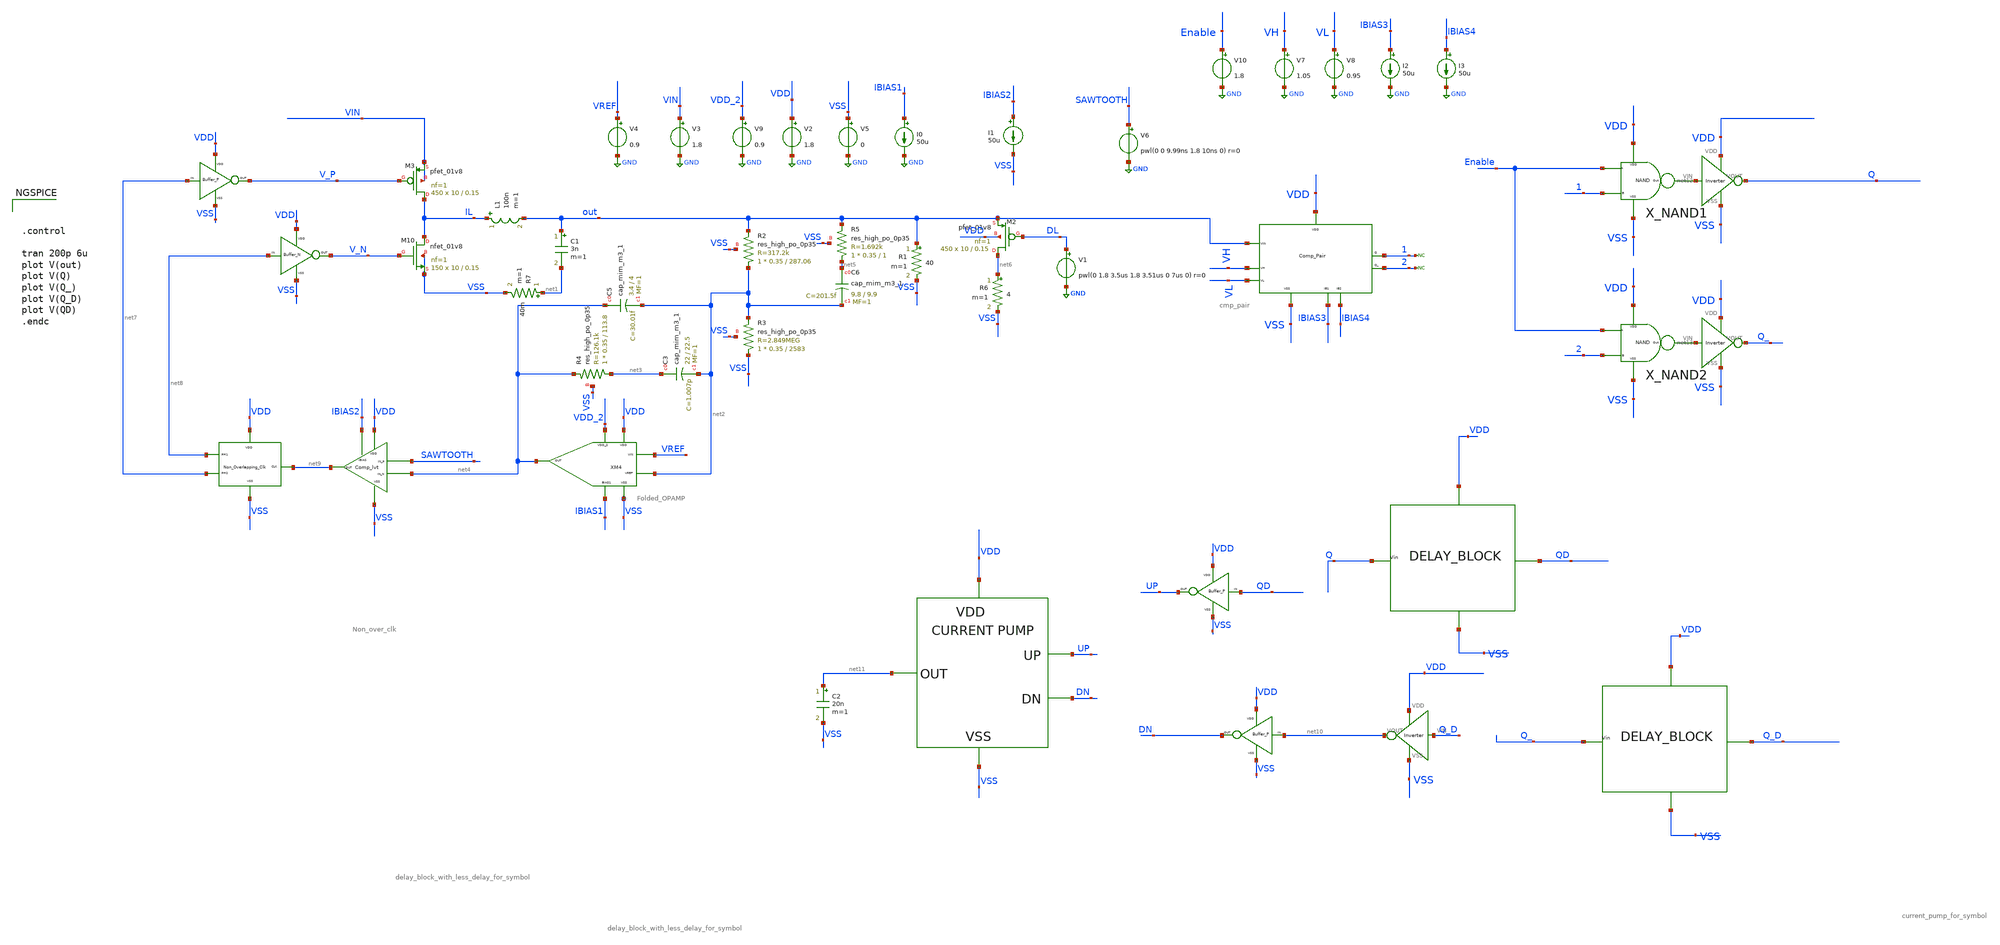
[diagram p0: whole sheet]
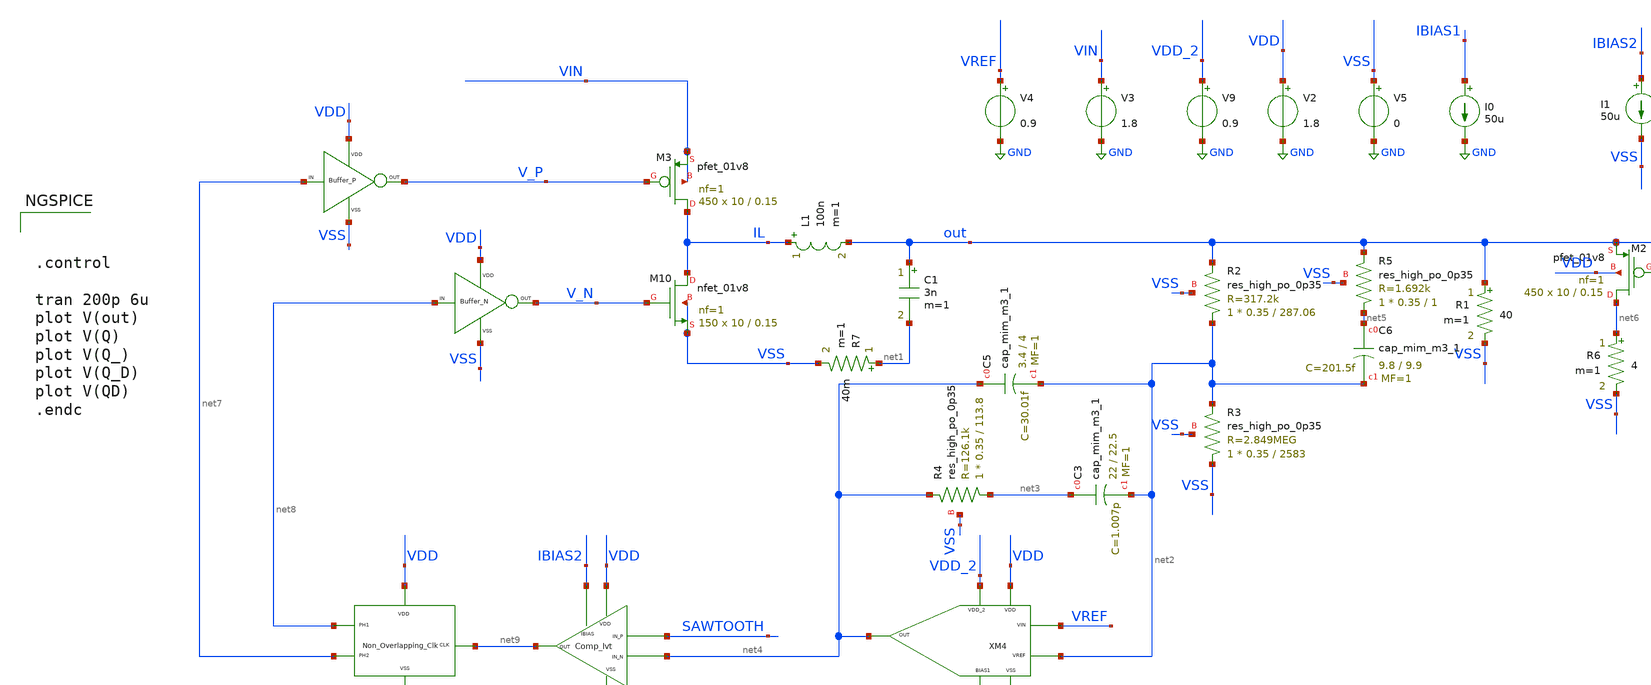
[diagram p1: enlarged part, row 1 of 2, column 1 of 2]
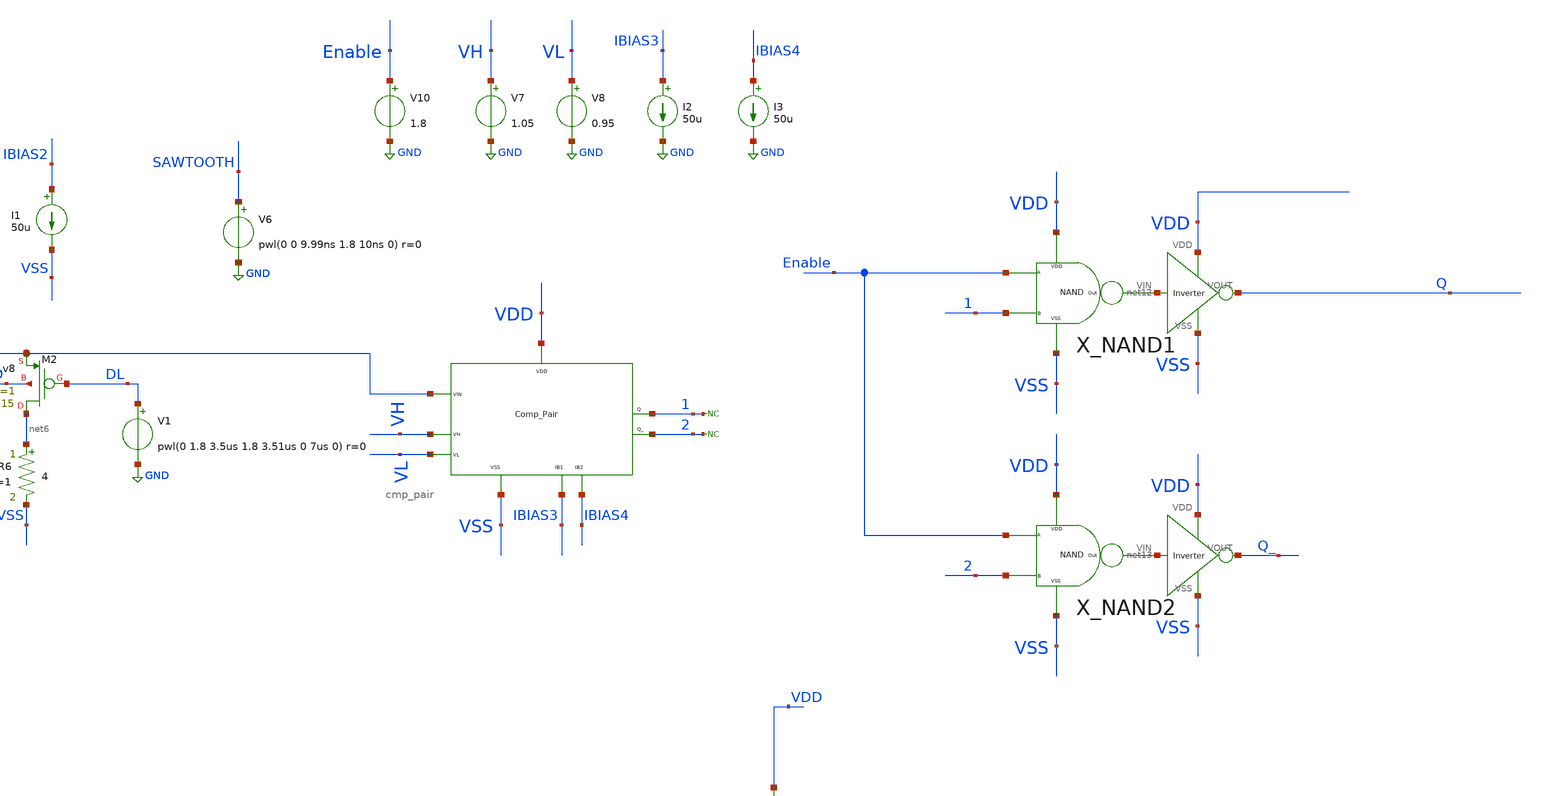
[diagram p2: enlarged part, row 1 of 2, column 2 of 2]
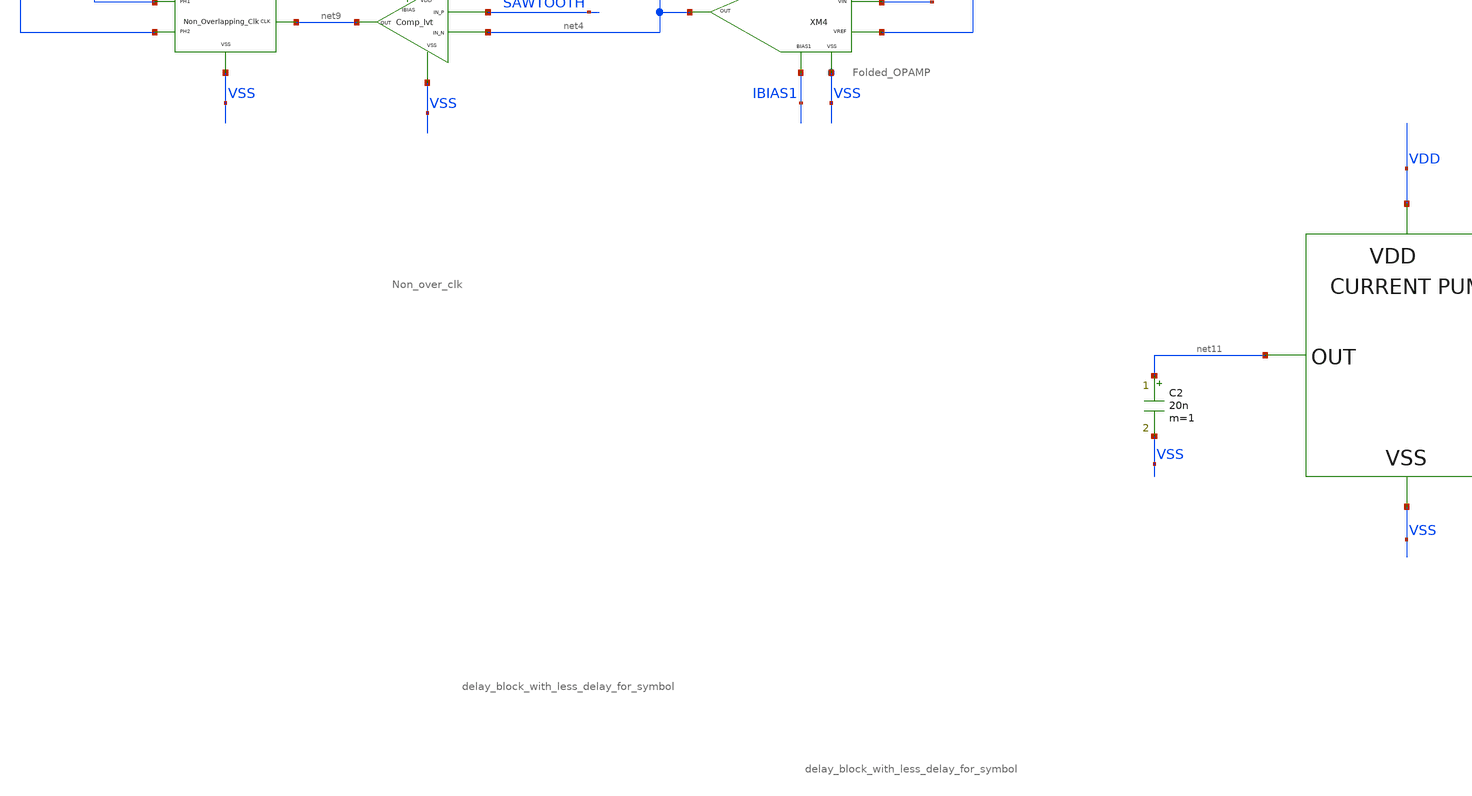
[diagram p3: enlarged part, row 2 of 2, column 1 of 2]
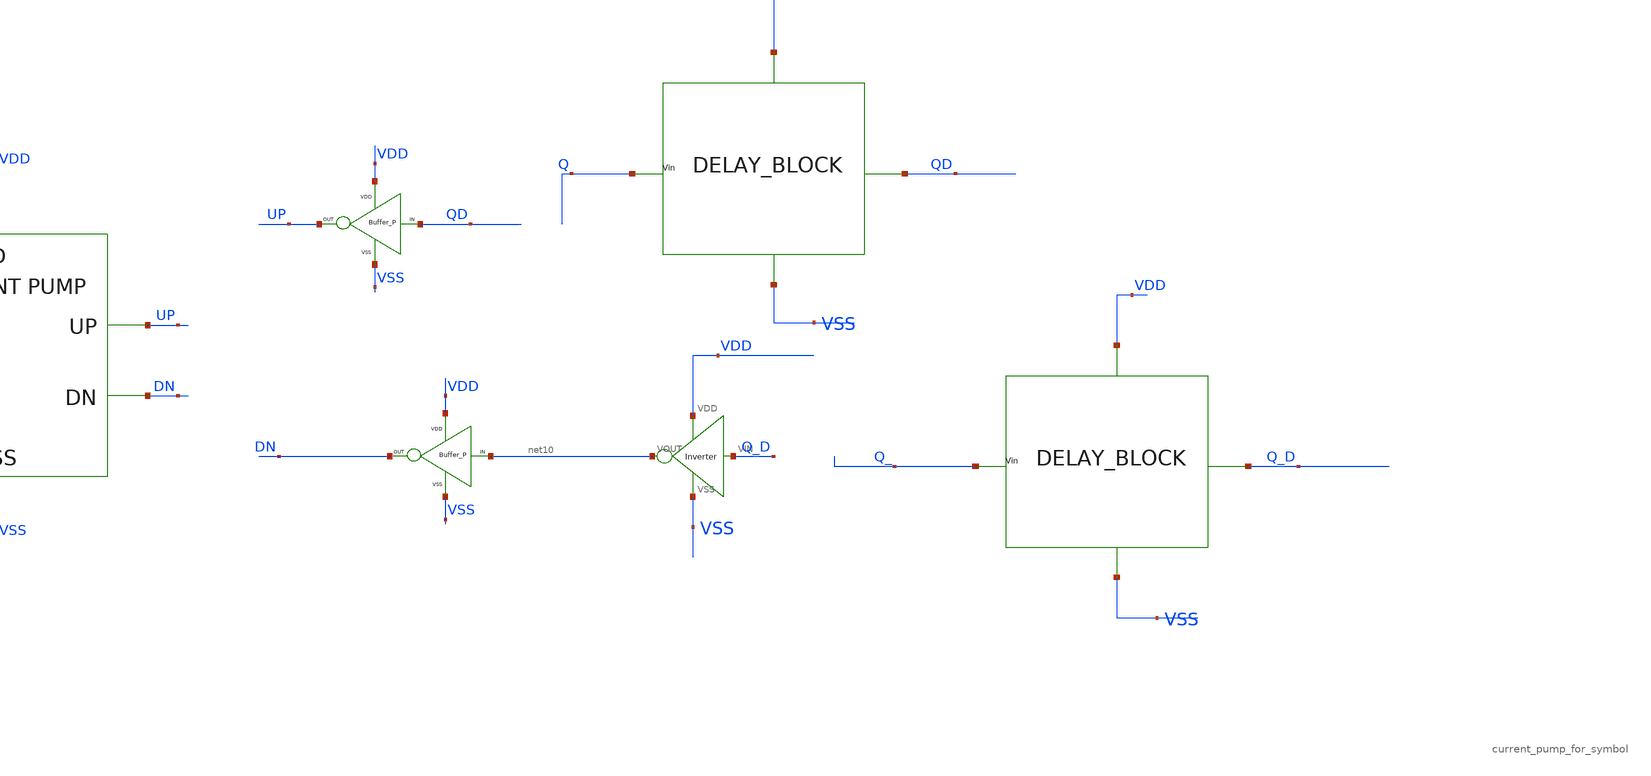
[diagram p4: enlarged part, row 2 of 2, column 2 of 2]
** sch_path: xschem/DC_DC_Converter_xschem/OTHERS/DC_DC_Converter_JV8/TOP_LEVEL/closed_loop_v14.sch
**.subckt closed_loop_v14
XM3 IL V_P VIN VIN sky130_fd_pr__pfet_01v8 L=0.15 W=10 nf=1 ad='int((nf+1)/2) * W/nf * 0.29' as='int((nf+2)/2) * W/nf * 0.29'
+ pd='2*int((nf+1)/2) * (W/nf + 0.29)' ps='2*int((nf+2)/2) * (W/nf + 0.29)' nrd='0.29 / W' nrs='0.29 / W'
+ sa=0 sb=0 sd=0 mult=450 m=450
L1 IL out 100n m=1
C1 out net1 3n m=1
V3 VIN GND 1.8
I0 IBIAS1 GND 50u
V9 VDD_2 GND 0.9
V2 VDD GND 1.8
V5 VSS GND 0
V4 VREF GND 0.9
I1 IBIAS2 VSS 50u
V6 SAWTOOTH GND pwl(0 0 9.99ns 1.8 10ns 0) r=0
XM2 net6 DL out VDD sky130_fd_pr__pfet_01v8 L=0.15 W=10 nf=1 ad='int((nf+1)/2) * W/nf * 0.29' as='int((nf+2)/2) * W/nf * 0.29'
+ pd='2*int((nf+1)/2) * (W/nf + 0.29)' ps='2*int((nf+2)/2) * (W/nf + 0.29)' nrd='0.29 / W' nrs='0.29 / W'
+ sa=0 sb=0 sd=0 mult=450 m=450
V1 DL GND pwl(0 1.8 3.5us 1.8 3.51us 0 7us 0) r=0
X1 net7 V_P VDD VSS BUFFER_P
X2 net8 V_N VDD VSS BUFFER_N
XM3 VDD net9 net8 VSS net7 Non_over_clk
XM4 VDD VSS VDD_2 IBIAS1 net4 VREF net2 Folded_OPAMP
XC5 net4 net2 sky130_fd_pr__cap_mim_m3_1 W=3.4 L=4 MF=1 m=1
XC3 net3 net2 sky130_fd_pr__cap_mim_m3_1 W=22 L=22.5 MF=1 m=1
XC6 net5 net2 sky130_fd_pr__cap_mim_m3_1 W=9.8 L=9.9 MF=1 m=1
XM10 IL V_N VSS VSS sky130_fd_pr__nfet_01v8 L=0.15 W=10 nf=1 ad='int((nf+1)/2) * W/nf * 0.29' as='int((nf+2)/2) * W/nf * 0.29'
+ pd='2*int((nf+1)/2) * (W/nf + 0.29)' ps='2*int((nf+2)/2) * (W/nf + 0.29)' nrd='0.29 / W' nrs='0.29 / W'
+ sa=0 sb=0 sd=0 mult=150 m=150
XR4 net3 net4 VSS sky130_fd_pr__res_high_po_0p35 L=113.8 mult=1 m=1
XR5 net5 out VSS sky130_fd_pr__res_high_po_0p35 L=1 mult=1 m=1
XR2 net2 out VSS sky130_fd_pr__res_high_po_0p35 L=287.06 mult=1 m=1
XR3 VSS net2 VSS sky130_fd_pr__res_high_po_0p35 L=2583 mult=1 m=1
R7 net1 VSS 40m m=1
R1 out VSS 40 m=1
R6 net6 VSS 4 m=1
XM1 VDD VSS out VH VL IBIAS3 IBIAS4 1 2 cmp_pair
V7 VH GND 1.05
V8 VL GND 0.95
I2 IBIAS3 GND 50u
I3 IBIAS4 GND 50u
* noconn 2
* noconn 1
X_NAND1 VDD VSS Enable 1 net12 NAND
X_NAND2 VDD VSS Enable 2 net13 NAND
X9 VSS VDD net12 Q Inverter
X10 VSS VDD net13 Q_ Inverter
V10 Enable GND 1.8
X5 net10 DN VDD VSS BUFFER_P
X6 QD UP VDD VSS BUFFER_P
X7 UP net11 VDD VSS DN current_pump_for_symbol
X3 VSS VDD Q_D net10 Inverter
C2 net11 VSS 20n m=1
X4 Q QD VDD VSS delay_block_with_less_delay_for_symbol
X8 Q_ Q_D VDD VSS delay_block_with_less_delay_for_symbol
XM2 IBIAS2 VDD SAWTOOTH net4 VSS net9 Comp_lvt
**** begin user architecture code

** opencircuitdesign pdks install
.lib $::SKYWATER_MODELS/sky130.lib.spice tt





.control

tran 200p 6u
plot V(out)
plot V(Q)
plot V(Q_)
plot V(Q_D)
plot V(QD)
.endc


**** end user architecture code
**.ends
.GLOBAL GND
.end
